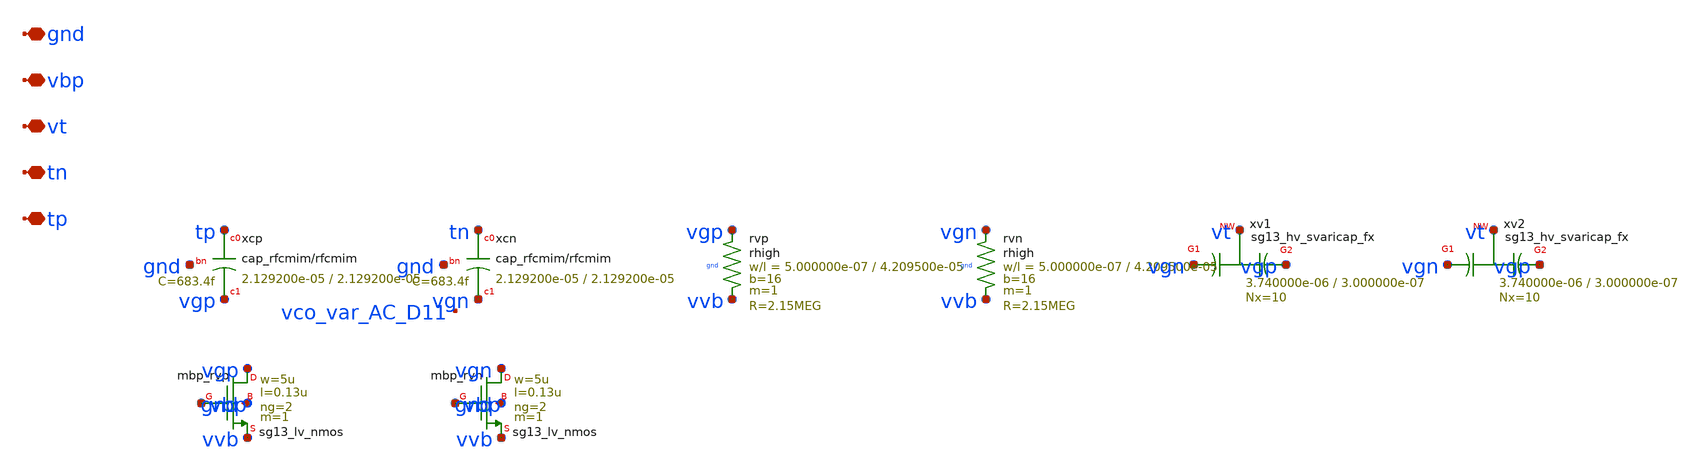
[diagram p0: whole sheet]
** sch_path: analog/vco/sch/vco_var.sch
**.subckt vco_var tp tn vt vbp gnd
*.iopin tp
*.iopin tn
*.iopin vt
*.iopin vbp
*.iopin gnd
Xxcp tp vgp gnd cap_rfcmim w=2.129200e-05 l=2.129200e-05 wfeed=5.0e-6 m=1 mm_ok=1
Xxcn tn vgn gnd cap_rfcmim w=2.129200e-05 l=2.129200e-05 wfeed=5.0e-6 m=1 mm_ok=1
Xrvp vgp vvb gnd rhigh w=5.000000e-07 l=4.209500e-05 m=1 b=16 mm_ok=1
Xrvn vgn vvb gnd rhigh w=5.000000e-07 l=4.209500e-05 m=1 b=16 mm_ok=1
Xxv1 vgn vt vgp sub! sg13_hv_svaricap_fx w=3.740000e-06 l=3.000000e-07 Nx=10 mm_ok=1
Xxv2 vgn vt vgp sub! sg13_hv_svaricap_fx w=3.740000e-06 l=3.000000e-07 Nx=10 mm_ok=1
Xmbp_rvp vgp vbp vvb gnd sg13_lv_nmos w=5u l=0.13u ng=2 m=1 mm_ok=1
Xmbp_rvn vgn vbp vvb gnd sg13_lv_nmos w=5u l=0.13u ng=2 m=1 mm_ok=1
**.ends
.end
